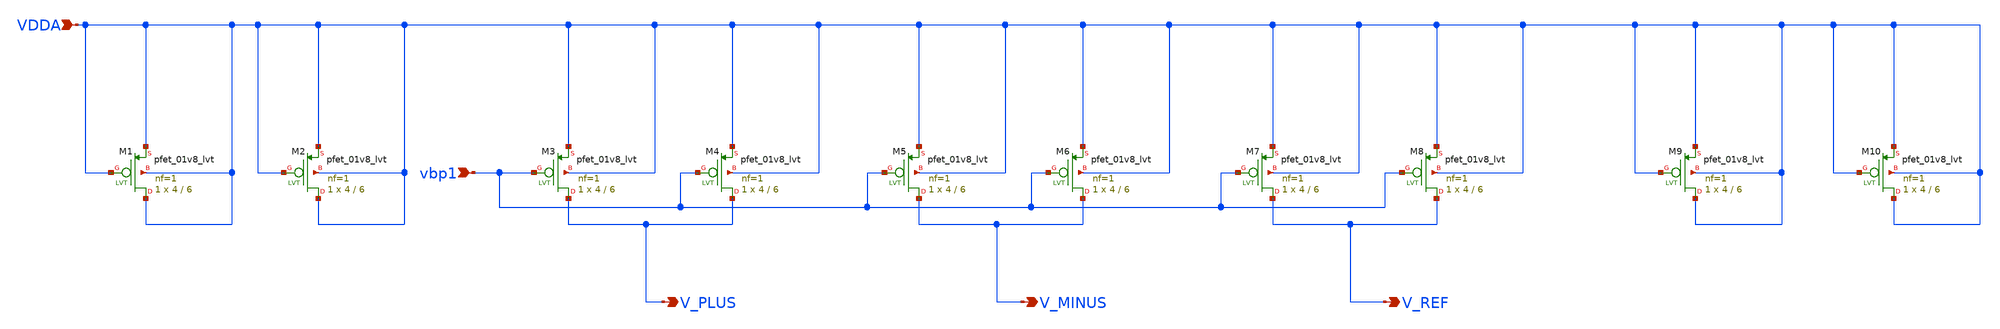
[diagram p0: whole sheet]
** sch_path: lef/lef/gds/bg2_currentmirror_xschem.sch
**.subckt bg2_currentmirror_xschem VDDA vbp1 V_PLUS V_MINUS V_REF
*.ipin VDDA
*.ipin vbp1
*.opin V_PLUS
*.opin V_MINUS
*.opin V_REF
XM9 VDDA VDDA VDDA VDDA sky130_fd_pr__pfet_01v8_lvt L=6 W=4 nf=1 ad='int((1 + 1)/2) * 4 / 1 * 0.29' as='int((1 + 2)/2) * 4 / 1 * 0.29'
+ pd='2*int((1 + 1)/2) * (4 / 1 + 0.29)' ps='2*int((1 + 2)/2) * (4 / 1 + 0.29)' nrd='0.29 / 4 ' nrs='0.29 / 4 '
+ sa=0 sb=0 sd=0 mult=1 m=1
XM3 V_PLUS vbp1 VDDA VDDA sky130_fd_pr__pfet_01v8_lvt L=6 W=4 nf=1 ad='int((1 + 1)/2) * 4 / 1 * 0.29'
+ as='int((1 + 2)/2) * 4 / 1 * 0.29' pd='2*int((1 + 1)/2) * (4 / 1 + 0.29)' ps='2*int((1 + 2)/2) * (4 / 1 + 0.29)'
+ nrd='0.29 / 4 ' nrs='0.29 / 4 ' sa=0 sb=0 sd=0 mult=1 m=1
XM1 VDDA VDDA VDDA VDDA sky130_fd_pr__pfet_01v8_lvt L=6 W=4 nf=1 ad='int((1 + 1)/2) * 4 / 1 * 0.29' as='int((1 + 2)/2) * 4 / 1 * 0.29'
+ pd='2*int((1 + 1)/2) * (4 / 1 + 0.29)' ps='2*int((1 + 2)/2) * (4 / 1 + 0.29)' nrd='0.29 / 4 ' nrs='0.29 / 4 '
+ sa=0 sb=0 sd=0 mult=1 m=1
XM2 VDDA VDDA VDDA VDDA sky130_fd_pr__pfet_01v8_lvt L=6 W=4 nf=1 ad='int((1 + 1)/2) * 4 / 1 * 0.29' as='int((1 + 2)/2) * 4 / 1 * 0.29'
+ pd='2*int((1 + 1)/2) * (4 / 1 + 0.29)' ps='2*int((1 + 2)/2) * (4 / 1 + 0.29)' nrd='0.29 / 4 ' nrs='0.29 / 4 '
+ sa=0 sb=0 sd=0 mult=1 m=1
XM10 VDDA VDDA VDDA VDDA sky130_fd_pr__pfet_01v8_lvt L=6 W=4 nf=1 ad='int((1 + 1)/2) * 4 / 1 * 0.29'
+ as='int((1 + 2)/2) * 4 / 1 * 0.29' pd='2*int((1 + 1)/2) * (4 / 1 + 0.29)' ps='2*int((1 + 2)/2) * (4 / 1 + 0.29)'
+ nrd='0.29 / 4 ' nrs='0.29 / 4 ' sa=0 sb=0 sd=0 mult=1 m=1
XM4 V_PLUS vbp1 VDDA VDDA sky130_fd_pr__pfet_01v8_lvt L=6 W=4 nf=1 ad='int((1 + 1)/2) * 4 / 1 * 0.29'
+ as='int((1 + 2)/2) * 4 / 1 * 0.29' pd='2*int((1 + 1)/2) * (4 / 1 + 0.29)' ps='2*int((1 + 2)/2) * (4 / 1 + 0.29)'
+ nrd='0.29 / 4 ' nrs='0.29 / 4 ' sa=0 sb=0 sd=0 mult=1 m=1
XM5 V_MINUS vbp1 VDDA VDDA sky130_fd_pr__pfet_01v8_lvt L=6 W=4 nf=1 ad='int((1 + 1)/2) * 4 / 1 * 0.29'
+ as='int((1 + 2)/2) * 4 / 1 * 0.29' pd='2*int((1 + 1)/2) * (4 / 1 + 0.29)' ps='2*int((1 + 2)/2) * (4 / 1 + 0.29)'
+ nrd='0.29 / 4 ' nrs='0.29 / 4 ' sa=0 sb=0 sd=0 mult=1 m=1
XM6 V_MINUS vbp1 VDDA VDDA sky130_fd_pr__pfet_01v8_lvt L=6 W=4 nf=1 ad='int((1 + 1)/2) * 4 / 1 * 0.29'
+ as='int((1 + 2)/2) * 4 / 1 * 0.29' pd='2*int((1 + 1)/2) * (4 / 1 + 0.29)' ps='2*int((1 + 2)/2) * (4 / 1 + 0.29)'
+ nrd='0.29 / 4 ' nrs='0.29 / 4 ' sa=0 sb=0 sd=0 mult=1 m=1
XM7 V_REF vbp1 VDDA VDDA sky130_fd_pr__pfet_01v8_lvt L=6 W=4 nf=1 ad='int((1 + 1)/2) * 4 / 1 * 0.29'
+ as='int((1 + 2)/2) * 4 / 1 * 0.29' pd='2*int((1 + 1)/2) * (4 / 1 + 0.29)' ps='2*int((1 + 2)/2) * (4 / 1 + 0.29)'
+ nrd='0.29 / 4 ' nrs='0.29 / 4 ' sa=0 sb=0 sd=0 mult=1 m=1
XM8 V_REF vbp1 VDDA VDDA sky130_fd_pr__pfet_01v8_lvt L=6 W=4 nf=1 ad='int((1 + 1)/2) * 4 / 1 * 0.29'
+ as='int((1 + 2)/2) * 4 / 1 * 0.29' pd='2*int((1 + 1)/2) * (4 / 1 + 0.29)' ps='2*int((1 + 2)/2) * (4 / 1 + 0.29)'
+ nrd='0.29 / 4 ' nrs='0.29 / 4 ' sa=0 sb=0 sd=0 mult=1 m=1
**.ends
.end
